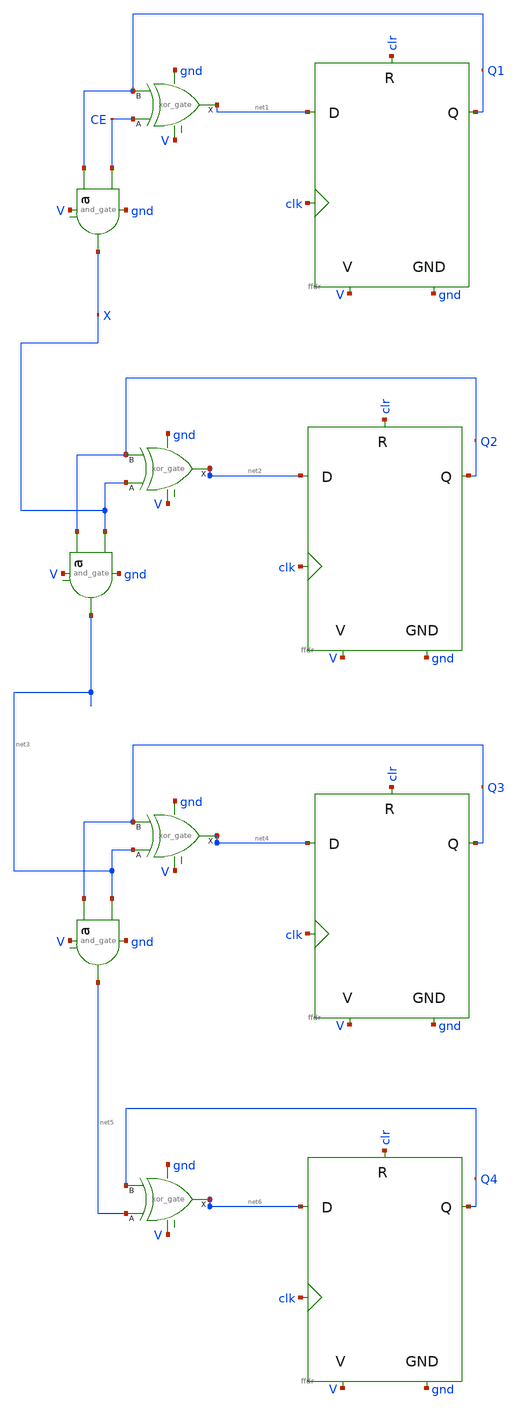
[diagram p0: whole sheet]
** sch_path: xschem/designs/counter4b/counter4bspi.sch
**.subckt counter4bspi
X1 Q1 CE gnd V X and_gate
X2 net1 clk V gnd Q1 clr ffdr
X3 CE Q1 net1 V gnd xor_gate
X5 net2 clk V gnd Q2 clr ffdr
X8 net4 clk V gnd Q3 clr ffdr
X11 net6 clk V gnd Q4 clr ffdr
X6 X Q2 net2 V gnd xor_gate
X9 net3 Q3 net4 V gnd xor_gate
X10 net5 Q4 net6 V gnd xor_gate
X4 Q2 X gnd V net3 and_gate
X7 Q3 net3 gnd V net5 and_gate
**.ends
.end
